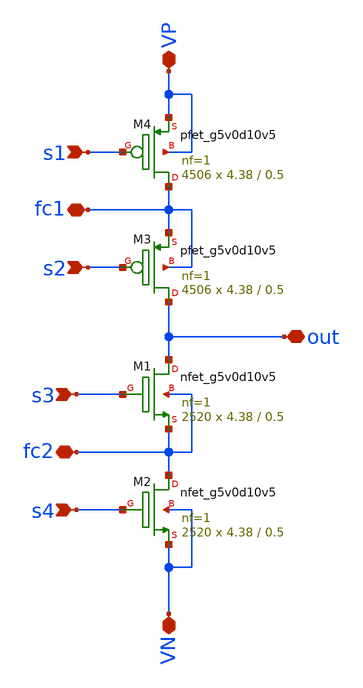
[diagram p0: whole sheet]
** sch_path: ISSCC23/submitted_notebooks/3LFCC/symbols/power_stage.sch
**.subckt power_stage VP s1 s2 out s3 s4 VN fc1 fc2
*.iopin VP
*.ipin s1
*.ipin s2
*.iopin out
*.ipin s3
*.ipin s4
*.iopin VN
*.iopin fc1
*.iopin fc2
XM3 out s2 fc1 fc1 sky130_fd_pr__pfet_g5v0d10v5 L=0.5 W=4.38 nf=1 ad='int((nf+1)/2) * W/nf * 0.29' as='int((nf+2)/2) * W/nf * 0.29'
+ pd='2*int((nf+1)/2) * (W/nf + 0.29)' ps='2*int((nf+2)/2) * (W/nf + 0.29)' nrd='0.29 / W' nrs='0.29 / W'
+ sa=0 sb=0 sd=0 mult=4506 m=4506
XM4 fc1 s1 VP VP sky130_fd_pr__pfet_g5v0d10v5 L=0.5 W=4.38 nf=1 ad='int((nf+1)/2) * W/nf * 0.29' as='int((nf+2)/2) * W/nf * 0.29'
+ pd='2*int((nf+1)/2) * (W/nf + 0.29)' ps='2*int((nf+2)/2) * (W/nf + 0.29)' nrd='0.29 / W' nrs='0.29 / W'
+ sa=0 sb=0 sd=0 mult=4506 m=4506
XM1 out s3 fc2 fc2 sky130_fd_pr__nfet_g5v0d10v5 L=0.5 W=4.38 nf=1 ad='int((nf+1)/2) * W/nf * 0.29' as='int((nf+2)/2) * W/nf * 0.29'
+ pd='2*int((nf+1)/2) * (W/nf + 0.29)' ps='2*int((nf+2)/2) * (W/nf + 0.29)' nrd='0.29 / W' nrs='0.29 / W'
+ sa=0 sb=0 sd=0 mult=2520 m=2520
XM2 fc2 s4 VN VN sky130_fd_pr__nfet_g5v0d10v5 L=0.5 W=4.38 nf=1 ad='int((nf+1)/2) * W/nf * 0.29' as='int((nf+2)/2) * W/nf * 0.29'
+ pd='2*int((nf+1)/2) * (W/nf + 0.29)' ps='2*int((nf+2)/2) * (W/nf + 0.29)' nrd='0.29 / W' nrs='0.29 / W'
+ sa=0 sb=0 sd=0 mult=2520 m=2520
**.ends
.end
